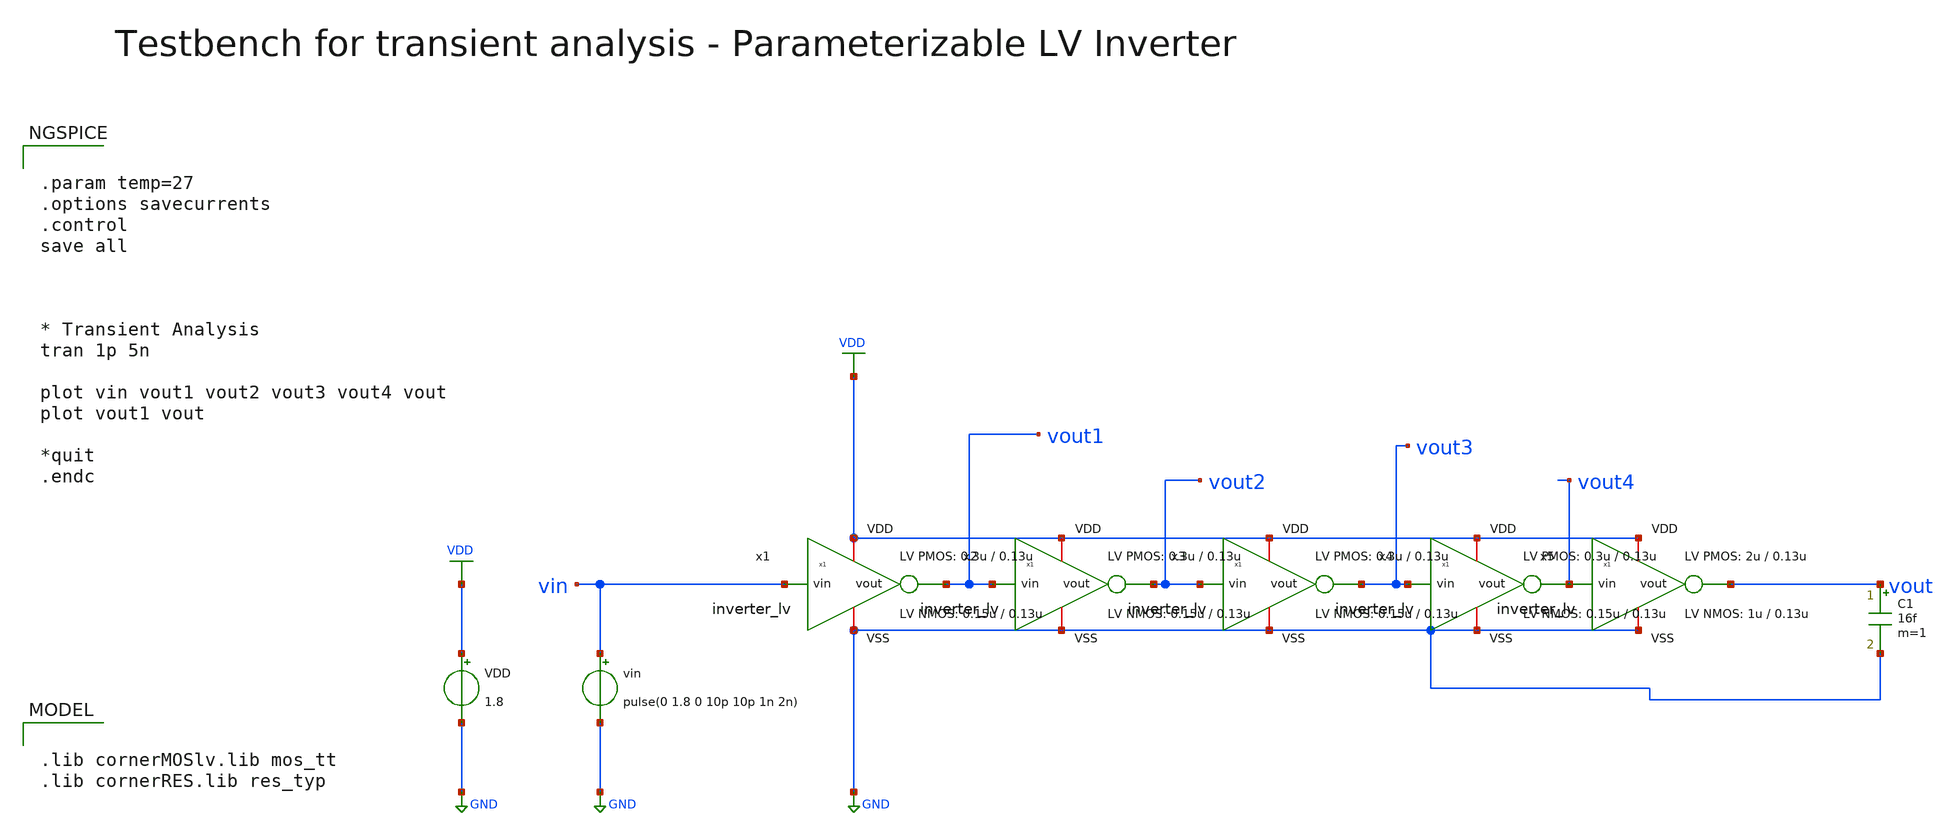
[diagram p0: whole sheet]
** sch_path: xschem/inverter/testbenches/inverter_lv_tb_tran.sch
**.subckt inverter_lv_tb_tran
VDD VDD GND 1.8
vin vin GND pulse(0 1.8 0 10p 10p 1n 2n)
x1 VDD vin vout1 GND inverter_lv W_P=0.3u L_P=0.13u W_N=0.15u L_N=0.13u N_C=1
x2 VDD vout1 vout2 GND inverter_lv W_P=0.3u L_P=0.13u W_N=0.15u L_N=0.13u N_C=1
x3 VDD vout2 vout3 GND inverter_lv W_P=0.3u L_P=0.13u W_N=0.15u L_N=0.13u N_C=1
x4 VDD vout3 vout4 GND inverter_lv W_P=0.3u L_P=0.13u W_N=0.15u L_N=0.13u N_C=1
C1 vout GND 16f m=1
x5 VDD vout4 vout GND inverter_lv W_P=2u L_P=0.13u W_N=1u L_N=0.13u N_C=1
**** begin user architecture code

.lib cornerMOSlv.lib mos_tt
.lib cornerRES.lib res_typ



.param temp=27
.options savecurrents
.control
save all



* Transient Analysis
tran 1p 5n

plot vin vout1 vout2 vout3 vout4 vout
plot vout1 vout

*quit
.endc


**** end user architecture code
**.ends

* expanding   symbol:  inverter/inverter_lv.sym # of pins=4
** sym_path: xschem/inverter/inverter_lv.sym
** sch_path: xschem/inverter/inverter_lv.sch
.subckt inverter_lv VDD vin vout VSS  W_P=3.0u L_P=0.13u W_N=1.0u L_N=0.13u N_C=1
*.ipin vin
*.iopin VDD
*.iopin VSS
*.opin vout
XM1 vout vin VDD VDD sg13_lv_pmos w=W_P l=L_P ng=1 m={N_C} mm_ok=1
XM2 vout vin VSS VSS sg13_lv_nmos w=W_N l=L_N ng=1 m={N_C} mm_ok=1
.ends

.GLOBAL GND
.GLOBAL VDD
.end
